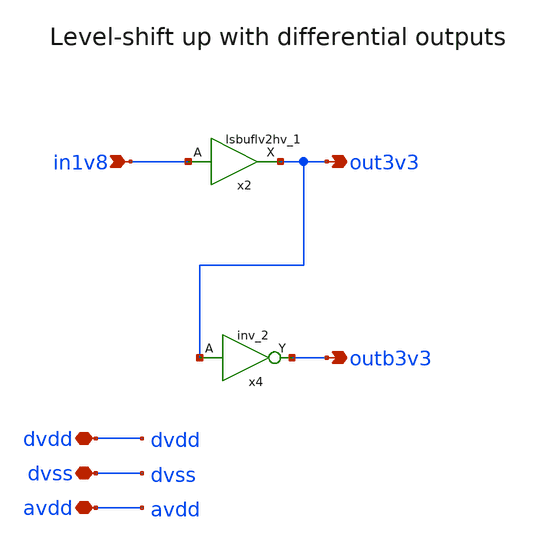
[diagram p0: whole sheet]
** sch_path: xschem/lvl_shift_invert.sch
**.subckt lvl_shift_invert in1v8 dvdd dvss avdd out3v3 outb3v3
*.ipin in1v8
*.iopin dvdd
*.iopin dvss
*.iopin avdd
*.opin out3v3
*.opin outb3v3
x2 in1v8 dvdd dvss dvss avdd avdd out3v3 sky130_fd_sc_hvl__lsbuflv2hv_1
x4 out3v3 dvss dvss avdd avdd outb3v3 sky130_fd_sc_hvl__inv_2
**.ends
.end
